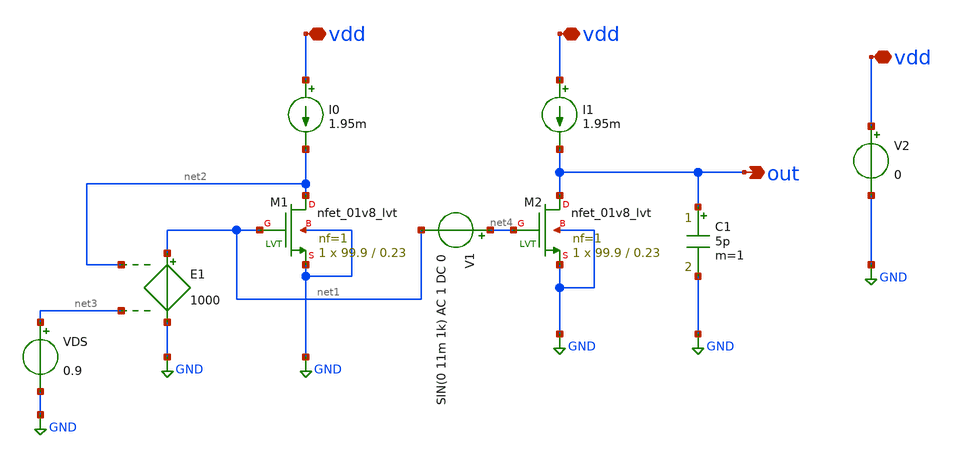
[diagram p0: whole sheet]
** sch_path: Simple-CS-Amplifier/csamp2.sch
**.subckt csamp2 vdd vdd vdd out
*.iopin vdd
*.iopin vdd
*.iopin vdd
*.opin out
XM1 net2 net1 GND GND sky130_fd_pr__nfet_01v8_lvt L=0.23 W=99.9 nf=1 ad='int((nf+1)/2) * W/nf * 0.29'
+ as='int((nf+2)/2) * W/nf * 0.29' pd='2*int((nf+1)/2) * (W/nf + 0.29)' ps='2*int((nf+2)/2) * (W/nf + 0.29)'
+ nrd='0.29 / W' nrs='0.29 / W' sa=0 sb=0 sd=0 mult=1 m=1
E1 net1 GND net2 net3 1000
I0 vdd net2 1.95m
VDS net3 GND 0.9
V2 vdd GND 0
XM2 out net4 GND GND sky130_fd_pr__nfet_01v8_lvt L=0.23 W=99.9 nf=1 ad='int((nf+1)/2) * W/nf * 0.29'
+ as='int((nf+2)/2) * W/nf * 0.29' pd='2*int((nf+1)/2) * (W/nf + 0.29)' ps='2*int((nf+2)/2) * (W/nf + 0.29)'
+ nrd='0.29 / W' nrs='0.29 / W' sa=0 sb=0 sd=0 mult=1 m=1
I1 vdd out 1.95m
V1 net4 net1 SIN(0 11m 1k) AC 1 DC 0
C1 out GND 5p m=1
**** begin user architecture code



.lib /usr/local/share/pdk/sky130A/libs.tech/ngspice/sky130.lib.spice tt
.option wnflag=1 scale=1e-6

.control
save all

*save @m.xm1.msky130_fd_pr__nfet_01v8_lvt[vgs]
*save @m.xm1.msky130_fd_pr__nfet_01v8_lvt[vds]

dc V1 -4m 4m 1u

*let vgs = @m.xm1.msky130_fd_pr__nfet_01v8_lvt[vgs]
*let vds = @m.xm1.msky130_fd_pr__nfet_01v8_lvt[vds]

*let a = deriv(vgs)
*let ao = -1/a

plot v(out)

*tran 10u 10m

*plot ao



*wrdata ao-L=0.40.txt ao
.endc


**** end user architecture code
**.ends
.GLOBAL GND
.end
